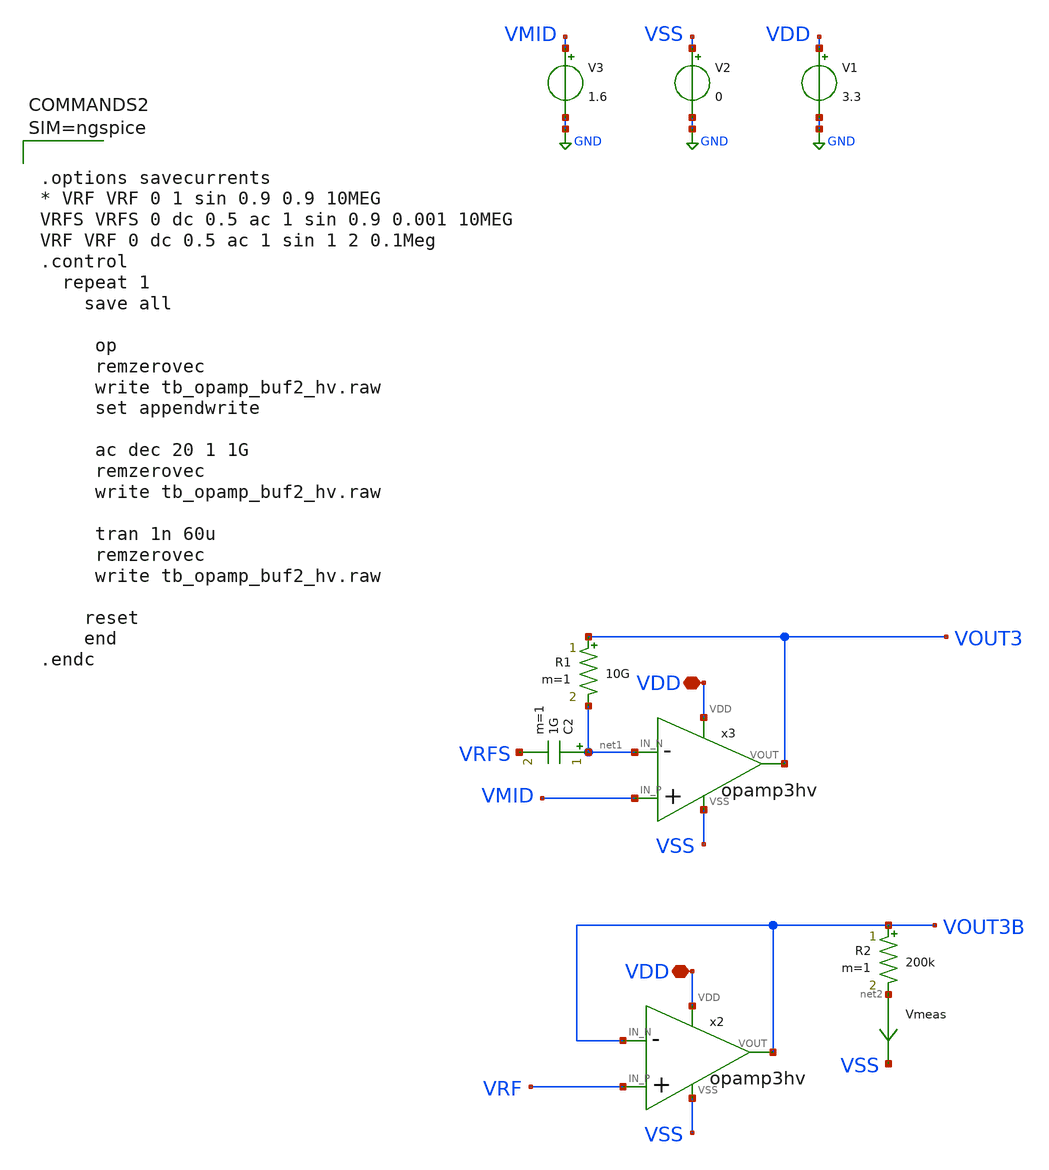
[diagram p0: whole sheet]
** sch_path: xschem/tb_opamp_buf2_hv.sch
**.subckt tb_opamp_buf2_hv VDD VDD
*.iopin VDD
*.iopin VDD
V1 VDD GND 3.3
V2 VSS GND 0
x3 VDD VMID net1 VOUT3 VSS opamp3hv
V3 VMID GND 1.6
C2 net1 VRFS 1G m=1
R1 VOUT3 net1 10G m=1
x2 VDD VRF VOUT3B VOUT3B VSS opamp3hv
R2 VOUT3B net2 200k m=1
Vmeas net2 VSS 0
.save i(vmeas)
**** begin user architecture code

** opencircuitdesign pdks install
.lib $::SKYWATER_MODELS/sky130.lib.spice tt





.options savecurrents
* VRF VRF 0 1 sin 0.9 0.9 10MEG
VRFS VRFS 0 dc 0.5 ac 1 sin 0.9 0.001 10MEG
VRF VRF 0 dc 0.5 ac 1 sin 1 2 0.1Meg
.control
  repeat 1
    save all

     op
     remzerovec
     write tb_opamp_buf2_hv.raw
     set appendwrite

     ac dec 20 1 1G
     remzerovec
     write tb_opamp_buf2_hv.raw

     tran 1n 60u
     remzerovec
     write tb_opamp_buf2_hv.raw

    reset
    end
.endc



**** end user architecture code
**.ends

* expanding   symbol:  opamp3hv.sym # of pins=5
** sym_path: xschem/opamp3hv.sym
** sch_path: xschem/opamp3hv.sch
.subckt opamp3hv VDD IN_P IN_N VOUT VSS
*.iopin VDD
*.iopin VSS
*.ipin IN_N
*.opin VOUT
*.ipin IN_P
vimeasn net2 VN 0
.save i(vimeasn)
vimeasp net3 voutstage1 0
.save i(vimeasp)
vicom vcom net1 0
.save i(vicom)
V3 vbias VSS 1.5
XC1 VOUT voutstage1 sky130_fd_pr__cap_mim_m3_1 W=1 L=1 MF=1 m=1
XM6 net1 vbias VSS VSS sky130_fd_pr__nfet_g5v0d10v5 L=1 W=2 nf=1 ad='int((nf+1)/2) * W/nf * 0.29' as='int((nf+2)/2) * W/nf * 0.29'
+ pd='2*int((nf+1)/2) * (W/nf + 0.29)' ps='2*int((nf+2)/2) * (W/nf + 0.29)' nrd='0.29 / W' nrs='0.29 / W'
+ sa=0 sb=0 sd=0 mult=1 m=1
XM8 net3 net2 VDD VDD sky130_fd_pr__pfet_g5v0d10v5 L=1 W=2 nf=1 ad='int((nf+1)/2) * W/nf * 0.29' as='int((nf+2)/2) * W/nf * 0.29'
+ pd='2*int((nf+1)/2) * (W/nf + 0.29)' ps='2*int((nf+2)/2) * (W/nf + 0.29)' nrd='0.29 / W' nrs='0.29 / W'
+ sa=0 sb=0 sd=0 mult=1 m=1
XM2 net2 net2 VDD VDD sky130_fd_pr__pfet_g5v0d10v5 L=1 W=2 nf=1 ad='int((nf+1)/2) * W/nf * 0.29' as='int((nf+2)/2) * W/nf * 0.29'
+ pd='2*int((nf+1)/2) * (W/nf + 0.29)' ps='2*int((nf+2)/2) * (W/nf + 0.29)' nrd='0.29 / W' nrs='0.29 / W'
+ sa=0 sb=0 sd=0 mult=1 m=1
XM1 VOUT voutstage1 VDD VDD sky130_fd_pr__pfet_g5v0d10v5 L=0.5 W=16 nf=1 ad='int((nf+1)/2) * W/nf * 0.29'
+ as='int((nf+2)/2) * W/nf * 0.29' pd='2*int((nf+1)/2) * (W/nf + 0.29)' ps='2*int((nf+2)/2) * (W/nf + 0.29)'
+ nrd='0.29 / W' nrs='0.29 / W' sa=0 sb=0 sd=0 mult=5 m=5
XM4 VOUT vbias VSS VSS sky130_fd_pr__nfet_g5v0d10v5 L=0.5 W=8 nf=1 ad='int((nf+1)/2) * W/nf * 0.29' as='int((nf+2)/2) * W/nf * 0.29'
+ pd='2*int((nf+1)/2) * (W/nf + 0.29)' ps='2*int((nf+2)/2) * (W/nf + 0.29)' nrd='0.29 / W' nrs='0.29 / W'
+ sa=0 sb=0 sd=0 mult=5 m=5
XM3 VN IN_N vcom VSS sky130_fd_pr__nfet_03v3_nvt L=0.5 W=4 nf=1 ad='int((nf+1)/2) * W/nf * 0.29' as='int((nf+2)/2) * W/nf * 0.29'
+ pd='2*int((nf+1)/2) * (W/nf + 0.29)' ps='2*int((nf+2)/2) * (W/nf + 0.29)' nrd='0.29 / W' nrs='0.29 / W'
+ sa=0 sb=0 sd=0 mult=4 m=4
XM5 voutstage1 IN_P vcom VSS sky130_fd_pr__nfet_03v3_nvt L=0.5 W=4 nf=1 ad='int((nf+1)/2) * W/nf * 0.29'
+ as='int((nf+2)/2) * W/nf * 0.29' pd='2*int((nf+1)/2) * (W/nf + 0.29)' ps='2*int((nf+2)/2) * (W/nf + 0.29)'
+ nrd='0.29 / W' nrs='0.29 / W' sa=0 sb=0 sd=0 mult=4 m=4
.ends

.GLOBAL GND
.end
